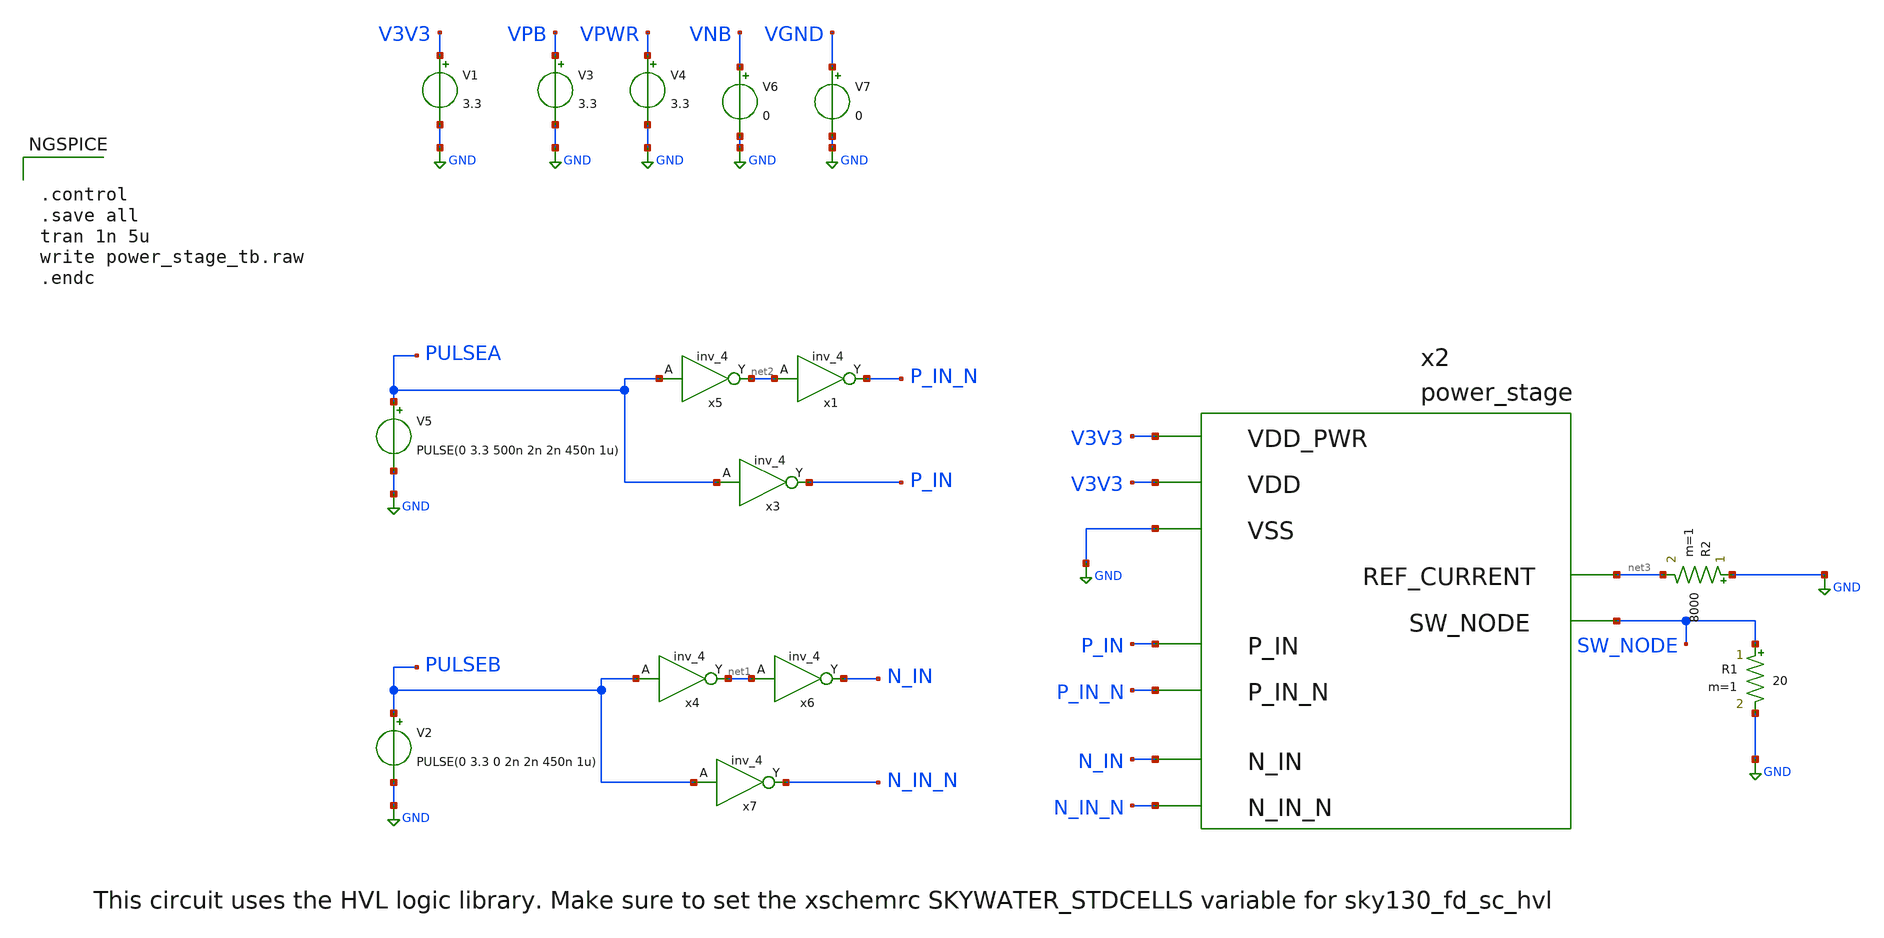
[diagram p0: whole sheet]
** sch_path: design/power-stage/power_stage_tb.sch
**.subckt power_stage_tb
V1 V3V3 GND 3.3
V2 PULSEB GND PULSE(0 3.3 0 2n 2n 450n 1u)
x2 V3V3 V3V3 GND P_IN P_IN_N N_IN net3 SW_NODE N_IN_N power_stage
V3 VPB GND 3.3
V4 VPWR GND 3.3
x5 PULSEA VGND VNB VPB VPWR net2 sky130_fd_sc_hvl__inv_4
V5 PULSEA GND PULSE(0 3.3 500n 2n 2n 450n 1u)
R1 SW_NODE GND 20 m=1
x1 net2 VGND VNB VPB VPWR P_IN_N sky130_fd_sc_hvl__inv_4
x3 PULSEA VGND VNB VPB VPWR P_IN sky130_fd_sc_hvl__inv_4
x4 PULSEB VGND VNB VPB VPWR net1 sky130_fd_sc_hvl__inv_4
x6 net1 VGND VNB VPB VPWR N_IN sky130_fd_sc_hvl__inv_4
x7 PULSEB VGND VNB VPB VPWR N_IN_N sky130_fd_sc_hvl__inv_4
R2 GND net3 8000 m=1
V6 VNB GND 0
V7 VGND GND 0
**** begin user architecture code


.control
.save all
tran 1n 5u
write power_stage_tb.raw
.endc



.include $::SKYWATER_MODELS/cells/nfet_01v8/sky130_fd_pr__nfet_01v8__tt.corner.spice
.include $::SKYWATER_MODELS/cells/nfet_01v8_lvt/sky130_fd_pr__nfet_01v8_lvt__tt.corner.spice
.include $::SKYWATER_MODELS/cells/pfet_01v8/sky130_fd_pr__pfet_01v8__tt.corner.spice
.include $::SKYWATER_MODELS/cells/nfet_03v3_nvt/sky130_fd_pr__nfet_03v3_nvt__tt.corner.spice
.include $::SKYWATER_MODELS/cells/nfet_05v0_nvt/sky130_fd_pr__nfet_05v0_nvt__tt.corner.spice
.include $::SKYWATER_MODELS/cells/esd_nfet_01v8/sky130_fd_pr__esd_nfet_01v8__tt.corner.spice
.include $::SKYWATER_MODELS/cells/pfet_01v8_lvt/sky130_fd_pr__pfet_01v8_lvt__tt.corner.spice
.include $::SKYWATER_MODELS/cells/pfet_01v8_hvt/sky130_fd_pr__pfet_01v8_hvt__tt.corner.spice
.include $::SKYWATER_MODELS/cells/esd_pfet_g5v0d10v5/sky130_fd_pr__esd_pfet_g5v0d10v5__tt.corner.spice
.include $::SKYWATER_MODELS/cells/pfet_g5v0d10v5/sky130_fd_pr__pfet_g5v0d10v5__tt.corner.spice
.include $::SKYWATER_MODELS/cells/pfet_g5v0d16v0/sky130_fd_pr__pfet_g5v0d16v0__tt.corner.spice
.include $::SKYWATER_MODELS/cells/nfet_g5v0d10v5/sky130_fd_pr__nfet_g5v0d10v5__tt.corner.spice
.include $::SKYWATER_MODELS/cells/nfet_g5v0d16v0/sky130_fd_pr__nfet_g5v0d16v0__tt_discrete.corner.spice
.include $::SKYWATER_MODELS/cells/esd_nfet_g5v0d10v5/sky130_fd_pr__esd_nfet_g5v0d10v5__tt.corner.spice
.include $::SKYWATER_MODELS/models/corners/tt/nonfet.spice
* Mismatch parameters
.include $::SKYWATER_MODELS/cells/nfet_01v8/sky130_fd_pr__nfet_01v8__mismatch.corner.spice
.include $::SKYWATER_MODELS/cells/pfet_01v8/sky130_fd_pr__pfet_01v8__mismatch.corner.spice
.include $::SKYWATER_MODELS/cells/nfet_01v8_lvt/sky130_fd_pr__nfet_01v8_lvt__mismatch.corner.spice
.include $::SKYWATER_MODELS/cells/pfet_01v8_lvt/sky130_fd_pr__pfet_01v8_lvt__mismatch.corner.spice
.include $::SKYWATER_MODELS/cells/pfet_01v8_hvt/sky130_fd_pr__pfet_01v8_hvt__mismatch.corner.spice
.include $::SKYWATER_MODELS/cells/nfet_g5v0d10v5/sky130_fd_pr__nfet_g5v0d10v5__mismatch.corner.spice
.include $::SKYWATER_MODELS/cells/pfet_g5v0d10v5/sky130_fd_pr__pfet_g5v0d10v5__mismatch.corner.spice
.include $::SKYWATER_MODELS/cells/nfet_05v0_nvt/sky130_fd_pr__nfet_05v0_nvt__mismatch.corner.spice
.include $::SKYWATER_MODELS/cells/nfet_03v3_nvt/sky130_fd_pr__nfet_03v3_nvt__mismatch.corner.spice
* Resistor$::SKYWATER_MODELS/Capacitor
.include $::SKYWATER_MODELS/models/r+c/res_typical__cap_typical.spice
.include $::SKYWATER_MODELS/models/r+c/res_typical__cap_typical__lin.spice
* Special cells
.include $::SKYWATER_MODELS/models/corners/tt/specialized_cells.spice
* All models
.include $::SKYWATER_MODELS/models/all.spice
* Corner
.include $::SKYWATER_MODELS/models/corners/tt/rf.spice

**** end user architecture code
**.ends

* expanding   symbol:  design/power-stage/power_stage.sym # of pins=9
** sym_path: design/power-stage/power_stage.sym
** sch_path: design/power-stage/power_stage.sch
.subckt power_stage VDD_PWR VDD VSS P_IN P_IN_N N_IN REF_CURRENT SW_NODE N_IN_N
*.ipin N_IN
*.ipin VSS
*.ipin VDD
*.ipin P_IN
*.ipin P_IN_N
*.ipin N_IN_N
*.ipin VDD_PWR
*.ipin REF_CURRENT
*.ipin SW_NODE
XM1 net1 N_IN VSS VSS sky130_fd_pr__nfet_g5v0d10v5 L=0.5 W=1 nf=1 ad='int((nf+1)/2) * W/nf * 0.29' as='int((nf+2)/2) * W/nf * 0.29'
+ pd='2*int((nf+1)/2) * (W/nf + 0.29)' ps='2*int((nf+2)/2) * (W/nf + 0.29)' nrd='0.29 / W' nrs='0.29 / W'
+ sa=0 sb=0 sd=0 mult=1 m=1
XM2 net1 S1_N VDD_PWR VDD_PWR sky130_fd_pr__pfet_g5v0d10v5 L=0.5 W=2 nf=1 ad='int((nf+1)/2) * W/nf * 0.29'
+ as='int((nf+2)/2) * W/nf * 0.29' pd='2*int((nf+1)/2) * (W/nf + 0.29)' ps='2*int((nf+2)/2) * (W/nf + 0.29)'
+ nrd='0.29 / W' nrs='0.29 / W' sa=0 sb=0 sd=0 mult=1 m=1
XM3 S1_N N_IN_N VSS VSS sky130_fd_pr__nfet_g5v0d10v5 L=0.5 W=1 nf=1 ad='int((nf+1)/2) * W/nf * 0.29'
+ as='int((nf+2)/2) * W/nf * 0.29' pd='2*int((nf+1)/2) * (W/nf + 0.29)' ps='2*int((nf+2)/2) * (W/nf + 0.29)'
+ nrd='0.29 / W' nrs='0.29 / W' sa=0 sb=0 sd=0 mult=1 m=1
XM4 S1_N net1 VDD_PWR VDD_PWR sky130_fd_pr__pfet_g5v0d10v5 L=0.5 W=2 nf=1 ad='int((nf+1)/2) * W/nf * 0.29'
+ as='int((nf+2)/2) * W/nf * 0.29' pd='2*int((nf+1)/2) * (W/nf + 0.29)' ps='2*int((nf+2)/2) * (W/nf + 0.29)'
+ nrd='0.29 / W' nrs='0.29 / W' sa=0 sb=0 sd=0 mult=1 m=1
XM5 S2_N S1_N VDD_PWR VDD_PWR sky130_fd_pr__pfet_g5v0d10v5 L=0.5 W=10 nf=1 ad='int((nf+1)/2) * W/nf * 0.29'
+ as='int((nf+2)/2) * W/nf * 0.29' pd='2*int((nf+1)/2) * (W/nf + 0.29)' ps='2*int((nf+2)/2) * (W/nf + 0.29)'
+ nrd='0.29 / W' nrs='0.29 / W' sa=0 sb=0 sd=0 mult=1 m=1
XM6 S2_N S1_N VSS VSS sky130_fd_pr__nfet_g5v0d10v5 L=0.5 W=5 nf=1 ad='int((nf+1)/2) * W/nf * 0.29' as='int((nf+2)/2) * W/nf * 0.29'
+ pd='2*int((nf+1)/2) * (W/nf + 0.29)' ps='2*int((nf+2)/2) * (W/nf + 0.29)' nrd='0.29 / W' nrs='0.29 / W'
+ sa=0 sb=0 sd=0 mult=1 m=1
XM7 S3_N S2_N VDD_PWR VDD_PWR sky130_fd_pr__pfet_g5v0d10v5 L=0.5 W=20 nf=1 ad='int((nf+1)/2) * W/nf * 0.29'
+ as='int((nf+2)/2) * W/nf * 0.29' pd='2*int((nf+1)/2) * (W/nf + 0.29)' ps='2*int((nf+2)/2) * (W/nf + 0.29)'
+ nrd='0.29 / W' nrs='0.29 / W' sa=0 sb=0 sd=0 mult=4 m=4
XM8 S3_N S2_N VSS VSS sky130_fd_pr__nfet_g5v0d10v5 L=0.5 W=20 nf=1 ad='int((nf+1)/2) * W/nf * 0.29' as='int((nf+2)/2) * W/nf * 0.29'
+ pd='2*int((nf+1)/2) * (W/nf + 0.29)' ps='2*int((nf+2)/2) * (W/nf + 0.29)' nrd='0.29 / W' nrs='0.29 / W'
+ sa=0 sb=0 sd=0 mult=2 m=2
XM9 S4_N S3_N VDD_PWR VDD_PWR sky130_fd_pr__pfet_g5v0d10v5 L=0.5 W=20 nf=1 ad='int((nf+1)/2) * W/nf * 0.29'
+ as='int((nf+2)/2) * W/nf * 0.29' pd='2*int((nf+1)/2) * (W/nf + 0.29)' ps='2*int((nf+2)/2) * (W/nf + 0.29)'
+ nrd='0.29 / W' nrs='0.29 / W' sa=0 sb=0 sd=0 mult=22 m=22
XM10 S4_N S3_N VSS VSS sky130_fd_pr__nfet_g5v0d10v5 L=0.5 W=20 nf=1 ad='int((nf+1)/2) * W/nf * 0.29'
+ as='int((nf+2)/2) * W/nf * 0.29' pd='2*int((nf+1)/2) * (W/nf + 0.29)' ps='2*int((nf+2)/2) * (W/nf + 0.29)'
+ nrd='0.29 / W' nrs='0.29 / W' sa=0 sb=0 sd=0 mult=11 m=11
XM11 N_DRIVE S4_N VDD_PWR VDD_PWR sky130_fd_pr__pfet_g5v0d10v5 L=0.5 W=20 nf=1 ad='int((nf+1)/2) * W/nf * 0.29'
+ as='int((nf+2)/2) * W/nf * 0.29' pd='2*int((nf+1)/2) * (W/nf + 0.29)' ps='2*int((nf+2)/2) * (W/nf + 0.29)'
+ nrd='0.29 / W' nrs='0.29 / W' sa=0 sb=0 sd=0 mult=120 m=120
XM12 N_DRIVE S4_N VSS VSS sky130_fd_pr__nfet_g5v0d10v5 L=0.5 W=20 nf=1 ad='int((nf+1)/2) * W/nf * 0.29'
+ as='int((nf+2)/2) * W/nf * 0.29' pd='2*int((nf+1)/2) * (W/nf + 0.29)' ps='2*int((nf+2)/2) * (W/nf + 0.29)'
+ nrd='0.29 / W' nrs='0.29 / W' sa=0 sb=0 sd=0 mult=60 m=60
XM13 SW_NODE N_DRIVE VSS VSS sky130_fd_pr__nfet_g5v0d10v5 L=0.5 W=20 nf=1 ad='int((nf+1)/2) * W/nf * 0.29'
+ as='int((nf+2)/2) * W/nf * 0.29' pd='2*int((nf+1)/2) * (W/nf + 0.29)' ps='2*int((nf+2)/2) * (W/nf + 0.29)'
+ nrd='0.29 / W' nrs='0.29 / W' sa=0 sb=0 sd=0 mult=400 m=400
XM14 SW_NODE P_DRIVE VDD_PWR VDD_PWR sky130_fd_pr__pfet_g5v0d10v5 L=0.5 W=20 nf=1 ad='int((nf+1)/2) * W/nf * 0.29'
+ as='int((nf+2)/2) * W/nf * 0.29' pd='2*int((nf+1)/2) * (W/nf + 0.29)' ps='2*int((nf+2)/2) * (W/nf + 0.29)'
+ nrd='0.29 / W' nrs='0.29 / W' sa=0 sb=0 sd=0 mult=800 m=800
XM15 REF_CURRENT P_DRIVE VDD_PWR VDD_PWR sky130_fd_pr__pfet_g5v0d10v5 L=0.5 W=20 nf=1 ad='int((nf+1)/2) * W/nf * 0.29'
+ as='int((nf+2)/2) * W/nf * 0.29' pd='2*int((nf+1)/2) * (W/nf + 0.29)' ps='2*int((nf+2)/2) * (W/nf + 0.29)'
+ nrd='0.29 / W' nrs='0.29 / W' sa=0 sb=0 sd=0 mult=2 m=2
XM16 net2 P_IN VSS VSS sky130_fd_pr__nfet_g5v0d10v5 L=0.5 W=1 nf=1 ad='int((nf+1)/2) * W/nf * 0.29' as='int((nf+2)/2) * W/nf * 0.29'
+ pd='2*int((nf+1)/2) * (W/nf + 0.29)' ps='2*int((nf+2)/2) * (W/nf + 0.29)' nrd='0.29 / W' nrs='0.29 / W'
+ sa=0 sb=0 sd=0 mult=1 m=1
XM17 net2 S1_P VDD_PWR VDD_PWR sky130_fd_pr__pfet_g5v0d10v5 L=0.5 W=2 nf=1 ad='int((nf+1)/2) * W/nf * 0.29'
+ as='int((nf+2)/2) * W/nf * 0.29' pd='2*int((nf+1)/2) * (W/nf + 0.29)' ps='2*int((nf+2)/2) * (W/nf + 0.29)'
+ nrd='0.29 / W' nrs='0.29 / W' sa=0 sb=0 sd=0 mult=1 m=1
XM18 S1_P P_IN_N VSS VSS sky130_fd_pr__nfet_g5v0d10v5 L=0.5 W=1 nf=1 ad='int((nf+1)/2) * W/nf * 0.29'
+ as='int((nf+2)/2) * W/nf * 0.29' pd='2*int((nf+1)/2) * (W/nf + 0.29)' ps='2*int((nf+2)/2) * (W/nf + 0.29)'
+ nrd='0.29 / W' nrs='0.29 / W' sa=0 sb=0 sd=0 mult=1 m=1
XM19 S1_P net2 VDD_PWR VDD_PWR sky130_fd_pr__pfet_g5v0d10v5 L=0.5 W=2 nf=1 ad='int((nf+1)/2) * W/nf * 0.29'
+ as='int((nf+2)/2) * W/nf * 0.29' pd='2*int((nf+1)/2) * (W/nf + 0.29)' ps='2*int((nf+2)/2) * (W/nf + 0.29)'
+ nrd='0.29 / W' nrs='0.29 / W' sa=0 sb=0 sd=0 mult=1 m=1
XM20 S2_P S1_P VDD_PWR VDD_PWR sky130_fd_pr__pfet_g5v0d10v5 L=0.5 W=10 nf=1 ad='int((nf+1)/2) * W/nf * 0.29'
+ as='int((nf+2)/2) * W/nf * 0.29' pd='2*int((nf+1)/2) * (W/nf + 0.29)' ps='2*int((nf+2)/2) * (W/nf + 0.29)'
+ nrd='0.29 / W' nrs='0.29 / W' sa=0 sb=0 sd=0 mult=1 m=1
XM21 S2_P S1_P VSS VSS sky130_fd_pr__nfet_g5v0d10v5 L=0.5 W=5 nf=1 ad='int((nf+1)/2) * W/nf * 0.29' as='int((nf+2)/2) * W/nf * 0.29'
+ pd='2*int((nf+1)/2) * (W/nf + 0.29)' ps='2*int((nf+2)/2) * (W/nf + 0.29)' nrd='0.29 / W' nrs='0.29 / W'
+ sa=0 sb=0 sd=0 mult=1 m=1
XM22 S3_P S2_P VDD_PWR VDD_PWR sky130_fd_pr__pfet_g5v0d10v5 L=0.5 W=20 nf=1 ad='int((nf+1)/2) * W/nf * 0.29'
+ as='int((nf+2)/2) * W/nf * 0.29' pd='2*int((nf+1)/2) * (W/nf + 0.29)' ps='2*int((nf+2)/2) * (W/nf + 0.29)'
+ nrd='0.29 / W' nrs='0.29 / W' sa=0 sb=0 sd=0 mult=4 m=4
XM23 S3_P S2_P VSS VSS sky130_fd_pr__nfet_g5v0d10v5 L=0.5 W=20 nf=1 ad='int((nf+1)/2) * W/nf * 0.29'
+ as='int((nf+2)/2) * W/nf * 0.29' pd='2*int((nf+1)/2) * (W/nf + 0.29)' ps='2*int((nf+2)/2) * (W/nf + 0.29)'
+ nrd='0.29 / W' nrs='0.29 / W' sa=0 sb=0 sd=0 mult=2 m=2
XM24 S4_P S3_P VDD_PWR VDD_PWR sky130_fd_pr__pfet_g5v0d10v5 L=0.5 W=20 nf=1 ad='int((nf+1)/2) * W/nf * 0.29'
+ as='int((nf+2)/2) * W/nf * 0.29' pd='2*int((nf+1)/2) * (W/nf + 0.29)' ps='2*int((nf+2)/2) * (W/nf + 0.29)'
+ nrd='0.29 / W' nrs='0.29 / W' sa=0 sb=0 sd=0 mult=22 m=22
XM25 S4_P S3_P VSS VSS sky130_fd_pr__nfet_g5v0d10v5 L=0.5 W=20 nf=1 ad='int((nf+1)/2) * W/nf * 0.29'
+ as='int((nf+2)/2) * W/nf * 0.29' pd='2*int((nf+1)/2) * (W/nf + 0.29)' ps='2*int((nf+2)/2) * (W/nf + 0.29)'
+ nrd='0.29 / W' nrs='0.29 / W' sa=0 sb=0 sd=0 mult=11 m=11
XM26 P_DRIVE S4_P VDD_PWR VDD_PWR sky130_fd_pr__pfet_g5v0d10v5 L=0.5 W=20 nf=1 ad='int((nf+1)/2) * W/nf * 0.29'
+ as='int((nf+2)/2) * W/nf * 0.29' pd='2*int((nf+1)/2) * (W/nf + 0.29)' ps='2*int((nf+2)/2) * (W/nf + 0.29)'
+ nrd='0.29 / W' nrs='0.29 / W' sa=0 sb=0 sd=0 mult=120 m=120
XM27 P_DRIVE S4_P VSS VSS sky130_fd_pr__nfet_g5v0d10v5 L=0.5 W=20 nf=1 ad='int((nf+1)/2) * W/nf * 0.29'
+ as='int((nf+2)/2) * W/nf * 0.29' pd='2*int((nf+1)/2) * (W/nf + 0.29)' ps='2*int((nf+2)/2) * (W/nf + 0.29)'
+ nrd='0.29 / W' nrs='0.29 / W' sa=0 sb=0 sd=0 mult=60 m=60
.ends

.GLOBAL GND
**** begin user architecture code
[sky130_models]
**** end user architecture code
.end
